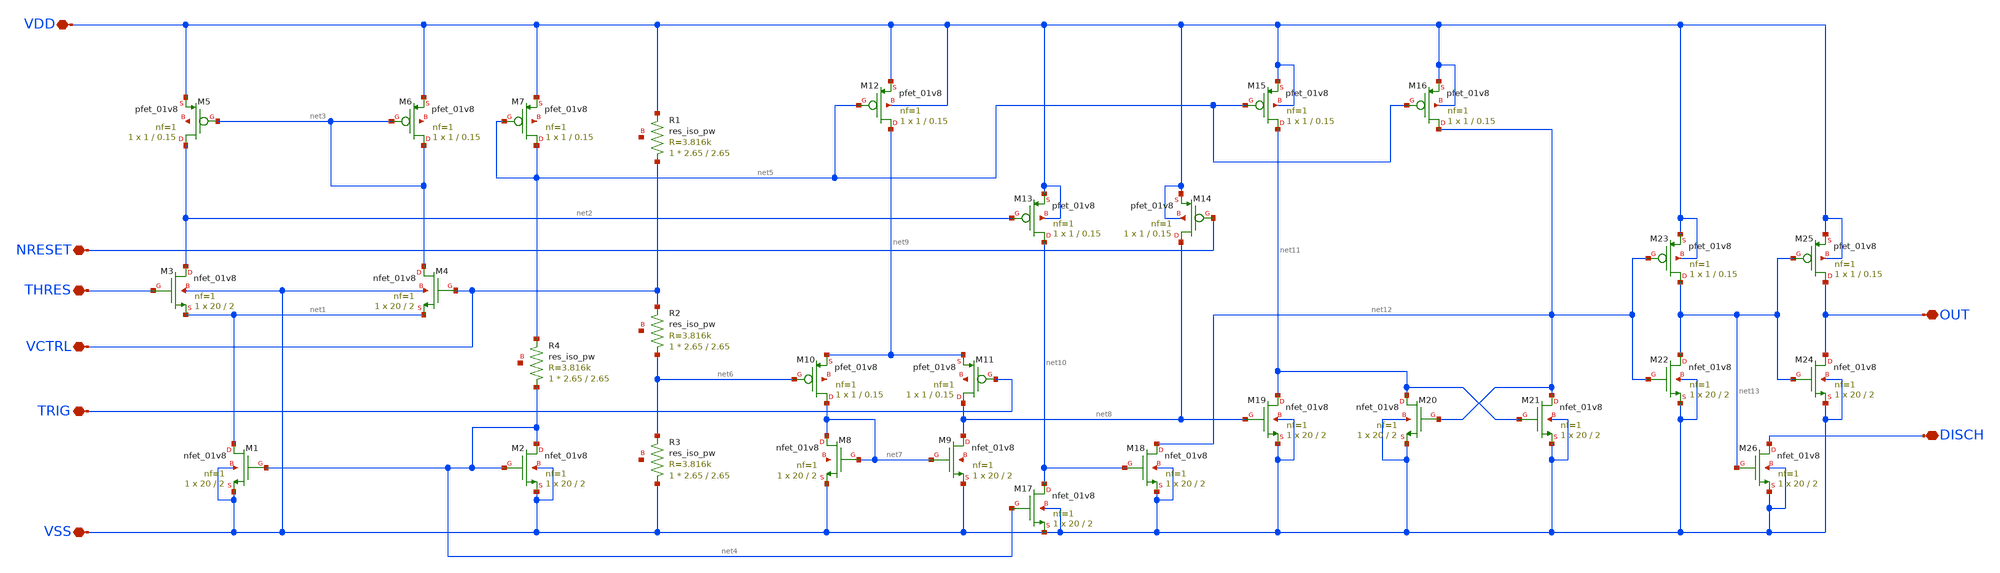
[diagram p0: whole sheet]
** sch_path: xschem/konsttimer.sch
**.subckt konsttimer VDD VSS DISCH VCTRL THRES TRIG NRESET OUT
*.iopin VDD
*.iopin VSS
*.iopin DISCH
*.iopin VCTRL
*.iopin THRES
*.iopin TRIG
*.iopin NRESET
*.iopin OUT
XR1 VCTRL VDD net14 sky130_fd_pr__res_iso_pw W=2.65 L=2.65 m=1
XR2 net6 VCTRL net15 sky130_fd_pr__res_iso_pw W=2.65 L=2.65 m=1
XR3 VSS net6 net16 sky130_fd_pr__res_iso_pw W=2.65 L=2.65 m=1
XM2 net4 net4 VSS VSS sky130_fd_pr__nfet_01v8 L=2 W=20 nf=1 ad='int((1 + 1)/2) * 20 / 1 * 0.29' as='int((1 + 2)/2) * 20 / 1 * 0.29'
+ pd='2*int((1 + 1)/2) * (20 / 1 + 0.29)' ps='2*int((1 + 2)/2) * (20 / 1 + 0.29)' nrd='0.29 / 20 ' nrs='0.29 / 20 '
+ sa=0 sb=0 sd=0 mult=1 m=1
XM1 net1 net4 VSS VSS sky130_fd_pr__nfet_01v8 L=2 W=20 nf=1 ad='int((1 + 1)/2) * 20 / 1 * 0.29' as='int((1 + 2)/2) * 20 / 1 * 0.29'
+ pd='2*int((1 + 1)/2) * (20 / 1 + 0.29)' ps='2*int((1 + 2)/2) * (20 / 1 + 0.29)' nrd='0.29 / 20 ' nrs='0.29 / 20 '
+ sa=0 sb=0 sd=0 mult=1 m=1
XM3 net2 THRES net1 VSS sky130_fd_pr__nfet_01v8 L=2 W=20 nf=1 ad='int((1 + 1)/2) * 20 / 1 * 0.29' as='int((1 + 2)/2) * 20 / 1 * 0.29'
+ pd='2*int((1 + 1)/2) * (20 / 1 + 0.29)' ps='2*int((1 + 2)/2) * (20 / 1 + 0.29)' nrd='0.29 / 20 ' nrs='0.29 / 20 '
+ sa=0 sb=0 sd=0 mult=1 m=1
XM4 net3 VCTRL net1 VSS sky130_fd_pr__nfet_01v8 L=2 W=20 nf=1 ad='int((1 + 1)/2) * 20 / 1 * 0.29' as='int((1 + 2)/2) * 20 / 1 * 0.29'
+ pd='2*int((1 + 1)/2) * (20 / 1 + 0.29)' ps='2*int((1 + 2)/2) * (20 / 1 + 0.29)' nrd='0.29 / 20 ' nrs='0.29 / 20 '
+ sa=0 sb=0 sd=0 mult=1 m=1
XM5 net2 net3 VDD net17 sky130_fd_pr__pfet_01v8 L=0.15 W=1 nf=1 ad='int((nf+1)/2) * W/nf * 0.29' as='int((nf+2)/2) * W/nf * 0.29'
+ pd='2*int((nf+1)/2) * (W/nf + 0.29)' ps='2*int((nf+2)/2) * (W/nf + 0.29)' nrd='0.29 / W' nrs='0.29 / W'
+ sa=0 sb=0 sd=0 mult=1 m=1
XM6 net3 net3 VDD net18 sky130_fd_pr__pfet_01v8 L=0.15 W=1 nf=1 ad='int((nf+1)/2) * W/nf * 0.29' as='int((nf+2)/2) * W/nf * 0.29'
+ pd='2*int((nf+1)/2) * (W/nf + 0.29)' ps='2*int((nf+2)/2) * (W/nf + 0.29)' nrd='0.29 / W' nrs='0.29 / W'
+ sa=0 sb=0 sd=0 mult=1 m=1
XM7 net5 net5 VDD net19 sky130_fd_pr__pfet_01v8 L=0.15 W=1 nf=1 ad='int((nf+1)/2) * W/nf * 0.29' as='int((nf+2)/2) * W/nf * 0.29'
+ pd='2*int((nf+1)/2) * (W/nf + 0.29)' ps='2*int((nf+2)/2) * (W/nf + 0.29)' nrd='0.29 / W' nrs='0.29 / W'
+ sa=0 sb=0 sd=0 mult=1 m=1
XR4 net4 net5 net20 sky130_fd_pr__res_iso_pw W=2.65 L=2.65 m=1
XM8 net7 net7 VSS net21 sky130_fd_pr__nfet_01v8 L=2 W=20 nf=1 ad='int((1 + 1)/2) * 20 / 1 * 0.29' as='int((1 + 2)/2) * 20 / 1 * 0.29'
+ pd='2*int((1 + 1)/2) * (20 / 1 + 0.29)' ps='2*int((1 + 2)/2) * (20 / 1 + 0.29)' nrd='0.29 / 20 ' nrs='0.29 / 20 '
+ sa=0 sb=0 sd=0 mult=1 m=1
XM9 net8 net7 VSS net22 sky130_fd_pr__nfet_01v8 L=2 W=20 nf=1 ad='int((1 + 1)/2) * 20 / 1 * 0.29' as='int((1 + 2)/2) * 20 / 1 * 0.29'
+ pd='2*int((1 + 1)/2) * (20 / 1 + 0.29)' ps='2*int((1 + 2)/2) * (20 / 1 + 0.29)' nrd='0.29 / 20 ' nrs='0.29 / 20 '
+ sa=0 sb=0 sd=0 mult=1 m=1
XM10 net7 net6 net9 net23 sky130_fd_pr__pfet_01v8 L=0.15 W=1 nf=1 ad='int((nf+1)/2) * W/nf * 0.29' as='int((nf+2)/2) * W/nf * 0.29'
+ pd='2*int((nf+1)/2) * (W/nf + 0.29)' ps='2*int((nf+2)/2) * (W/nf + 0.29)' nrd='0.29 / W' nrs='0.29 / W'
+ sa=0 sb=0 sd=0 mult=1 m=1
XM11 net8 TRIG net9 net24 sky130_fd_pr__pfet_01v8 L=0.15 W=1 nf=1 ad='int((nf+1)/2) * W/nf * 0.29' as='int((nf+2)/2) * W/nf * 0.29'
+ pd='2*int((nf+1)/2) * (W/nf + 0.29)' ps='2*int((nf+2)/2) * (W/nf + 0.29)' nrd='0.29 / W' nrs='0.29 / W'
+ sa=0 sb=0 sd=0 mult=1 m=1
XM12 net9 net5 VDD VDD sky130_fd_pr__pfet_01v8 L=0.15 W=1 nf=1 ad='int((nf+1)/2) * W/nf * 0.29' as='int((nf+2)/2) * W/nf * 0.29'
+ pd='2*int((nf+1)/2) * (W/nf + 0.29)' ps='2*int((nf+2)/2) * (W/nf + 0.29)' nrd='0.29 / W' nrs='0.29 / W'
+ sa=0 sb=0 sd=0 mult=1 m=1
XM13 net10 net2 VDD VDD sky130_fd_pr__pfet_01v8 L=0.15 W=1 nf=1 ad='int((nf+1)/2) * W/nf * 0.29' as='int((nf+2)/2) * W/nf * 0.29'
+ pd='2*int((nf+1)/2) * (W/nf + 0.29)' ps='2*int((nf+2)/2) * (W/nf + 0.29)' nrd='0.29 / W' nrs='0.29 / W'
+ sa=0 sb=0 sd=0 mult=1 m=1
XM14 net8 NRESET VDD VDD sky130_fd_pr__pfet_01v8 L=0.15 W=1 nf=1 ad='int((nf+1)/2) * W/nf * 0.29' as='int((nf+2)/2) * W/nf * 0.29'
+ pd='2*int((nf+1)/2) * (W/nf + 0.29)' ps='2*int((nf+2)/2) * (W/nf + 0.29)' nrd='0.29 / W' nrs='0.29 / W'
+ sa=0 sb=0 sd=0 mult=1 m=1
XM15 net11 net5 VDD VDD sky130_fd_pr__pfet_01v8 L=0.15 W=1 nf=1 ad='int((nf+1)/2) * W/nf * 0.29' as='int((nf+2)/2) * W/nf * 0.29'
+ pd='2*int((nf+1)/2) * (W/nf + 0.29)' ps='2*int((nf+2)/2) * (W/nf + 0.29)' nrd='0.29 / W' nrs='0.29 / W'
+ sa=0 sb=0 sd=0 mult=1 m=1
XM16 net12 net5 VDD VDD sky130_fd_pr__pfet_01v8 L=0.15 W=1 nf=1 ad='int((nf+1)/2) * W/nf * 0.29' as='int((nf+2)/2) * W/nf * 0.29'
+ pd='2*int((nf+1)/2) * (W/nf + 0.29)' ps='2*int((nf+2)/2) * (W/nf + 0.29)' nrd='0.29 / W' nrs='0.29 / W'
+ sa=0 sb=0 sd=0 mult=1 m=1
XM17 net10 net4 VSS VSS sky130_fd_pr__nfet_01v8 L=2 W=20 nf=1 ad='int((1 + 1)/2) * 20 / 1 * 0.29' as='int((1 + 2)/2) * 20 / 1 * 0.29'
+ pd='2*int((1 + 1)/2) * (20 / 1 + 0.29)' ps='2*int((1 + 2)/2) * (20 / 1 + 0.29)' nrd='0.29 / 20 ' nrs='0.29 / 20 '
+ sa=0 sb=0 sd=0 mult=1 m=1
XM18 net12 net10 VSS VSS sky130_fd_pr__nfet_01v8 L=2 W=20 nf=1 ad='int((1 + 1)/2) * 20 / 1 * 0.29' as='int((1 + 2)/2) * 20 / 1 * 0.29'
+ pd='2*int((1 + 1)/2) * (20 / 1 + 0.29)' ps='2*int((1 + 2)/2) * (20 / 1 + 0.29)' nrd='0.29 / 20 ' nrs='0.29 / 20 '
+ sa=0 sb=0 sd=0 mult=1 m=1
XM19 net11 net8 VSS VSS sky130_fd_pr__nfet_01v8 L=2 W=20 nf=1 ad='int((1 + 1)/2) * 20 / 1 * 0.29' as='int((1 + 2)/2) * 20 / 1 * 0.29'
+ pd='2*int((1 + 1)/2) * (20 / 1 + 0.29)' ps='2*int((1 + 2)/2) * (20 / 1 + 0.29)' nrd='0.29 / 20 ' nrs='0.29 / 20 '
+ sa=0 sb=0 sd=0 mult=1 m=1
XM20 net11 net12 VSS VSS sky130_fd_pr__nfet_01v8 L=2 W=20 nf=1 ad='int((1 + 1)/2) * 20 / 1 * 0.29' as='int((1 + 2)/2) * 20 / 1 * 0.29'
+ pd='2*int((1 + 1)/2) * (20 / 1 + 0.29)' ps='2*int((1 + 2)/2) * (20 / 1 + 0.29)' nrd='0.29 / 20 ' nrs='0.29 / 20 '
+ sa=0 sb=0 sd=0 mult=1 m=1
XM21 net12 net11 VSS VSS sky130_fd_pr__nfet_01v8 L=2 W=20 nf=1 ad='int((1 + 1)/2) * 20 / 1 * 0.29' as='int((1 + 2)/2) * 20 / 1 * 0.29'
+ pd='2*int((1 + 1)/2) * (20 / 1 + 0.29)' ps='2*int((1 + 2)/2) * (20 / 1 + 0.29)' nrd='0.29 / 20 ' nrs='0.29 / 20 '
+ sa=0 sb=0 sd=0 mult=1 m=1
XM22 net13 net12 VSS VSS sky130_fd_pr__nfet_01v8 L=2 W=20 nf=1 ad='int((1 + 1)/2) * 20 / 1 * 0.29' as='int((1 + 2)/2) * 20 / 1 * 0.29'
+ pd='2*int((1 + 1)/2) * (20 / 1 + 0.29)' ps='2*int((1 + 2)/2) * (20 / 1 + 0.29)' nrd='0.29 / 20 ' nrs='0.29 / 20 '
+ sa=0 sb=0 sd=0 mult=1 m=1
XM23 net13 net12 VDD VDD sky130_fd_pr__pfet_01v8 L=0.15 W=1 nf=1 ad='int((nf+1)/2) * W/nf * 0.29' as='int((nf+2)/2) * W/nf * 0.29'
+ pd='2*int((nf+1)/2) * (W/nf + 0.29)' ps='2*int((nf+2)/2) * (W/nf + 0.29)' nrd='0.29 / W' nrs='0.29 / W'
+ sa=0 sb=0 sd=0 mult=1 m=1
XM24 OUT net13 VSS VSS sky130_fd_pr__nfet_01v8 L=2 W=20 nf=1 ad='int((1 + 1)/2) * 20 / 1 * 0.29' as='int((1 + 2)/2) * 20 / 1 * 0.29'
+ pd='2*int((1 + 1)/2) * (20 / 1 + 0.29)' ps='2*int((1 + 2)/2) * (20 / 1 + 0.29)' nrd='0.29 / 20 ' nrs='0.29 / 20 '
+ sa=0 sb=0 sd=0 mult=1 m=1
XM25 OUT net13 VDD VDD sky130_fd_pr__pfet_01v8 L=0.15 W=1 nf=1 ad='int((nf+1)/2) * W/nf * 0.29' as='int((nf+2)/2) * W/nf * 0.29'
+ pd='2*int((nf+1)/2) * (W/nf + 0.29)' ps='2*int((nf+2)/2) * (W/nf + 0.29)' nrd='0.29 / W' nrs='0.29 / W'
+ sa=0 sb=0 sd=0 mult=1 m=1
XM26 DISCH net13 VSS VSS sky130_fd_pr__nfet_01v8 L=2 W=20 nf=1 ad='int((1 + 1)/2) * 20 / 1 * 0.29' as='int((1 + 2)/2) * 20 / 1 * 0.29'
+ pd='2*int((1 + 1)/2) * (20 / 1 + 0.29)' ps='2*int((1 + 2)/2) * (20 / 1 + 0.29)' nrd='0.29 / 20 ' nrs='0.29 / 20 '
+ sa=0 sb=0 sd=0 mult=1 m=1
**.ends
.end
